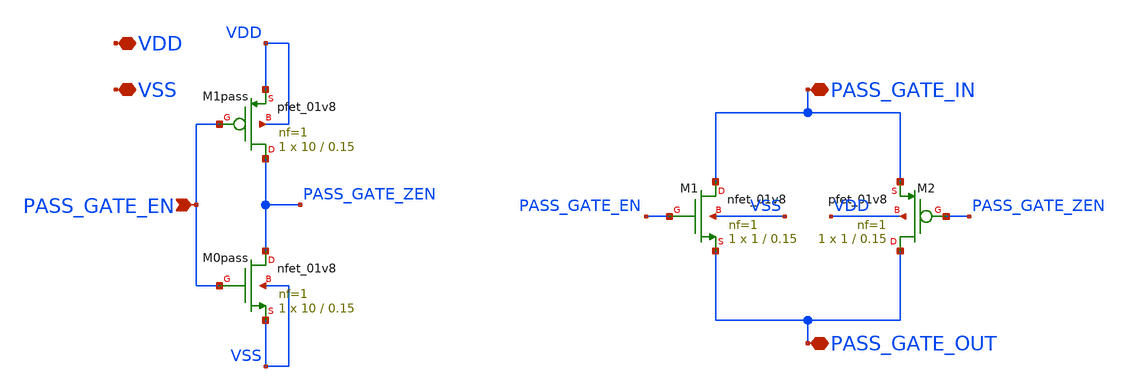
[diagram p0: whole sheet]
** sch_path: xschem/PASSGATE.sch
**.subckt PASSGATE PASS_GATE_IN PASS_GATE_EN VDD VSS PASS_GATE_OUT
*.iopin PASS_GATE_IN
*.ipin PASS_GATE_EN
*.iopin VDD
*.iopin VSS
*.iopin PASS_GATE_OUT
XM1pass PASS_GATE_ZEN PASS_GATE_EN VDD VDD sky130_fd_pr__pfet_01v8 L=0.15 W=10 nf=1 ad='int((nf+1)/2) * W/nf * 0.29'
+ as='int((nf+2)/2) * W/nf * 0.29' pd='2*int((nf+1)/2) * (W/nf + 0.29)' ps='2*int((nf+2)/2) * (W/nf + 0.29)'
+ nrd='0.29 / W' nrs='0.29 / W' sa=0 sb=0 sd=0 mult=1 m=1
XM0pass PASS_GATE_ZEN PASS_GATE_EN VSS VSS sky130_fd_pr__nfet_01v8 L=0.15 W=10 nf=1 ad='int((nf+1)/2) * W/nf * 0.29'
+ as='int((nf+2)/2) * W/nf * 0.29' pd='2*int((nf+1)/2) * (W/nf + 0.29)' ps='2*int((nf+2)/2) * (W/nf + 0.29)'
+ nrd='0.29 / W' nrs='0.29 / W' sa=0 sb=0 sd=0 mult=1 m=1
XM1 PASS_GATE_IN PASS_GATE_EN PASS_GATE_OUT VSS sky130_fd_pr__nfet_01v8 L=0.15 W=1 nf=1 ad='int((nf+1)/2) * W/nf * 0.29'
+ as='int((nf+2)/2) * W/nf * 0.29' pd='2*int((nf+1)/2) * (W/nf + 0.29)' ps='2*int((nf+2)/2) * (W/nf + 0.29)'
+ nrd='0.29 / W' nrs='0.29 / W' sa=0 sb=0 sd=0 mult=1 m=1
XM2 PASS_GATE_OUT PASS_GATE_ZEN PASS_GATE_IN VDD sky130_fd_pr__pfet_01v8 L=0.15 W=1 nf=1 ad='int((nf+1)/2) * W/nf * 0.29'
+ as='int((nf+2)/2) * W/nf * 0.29' pd='2*int((nf+1)/2) * (W/nf + 0.29)' ps='2*int((nf+2)/2) * (W/nf + 0.29)'
+ nrd='0.29 / W' nrs='0.29 / W' sa=0 sb=0 sd=0 mult=1 m=1
**.ends
.end
